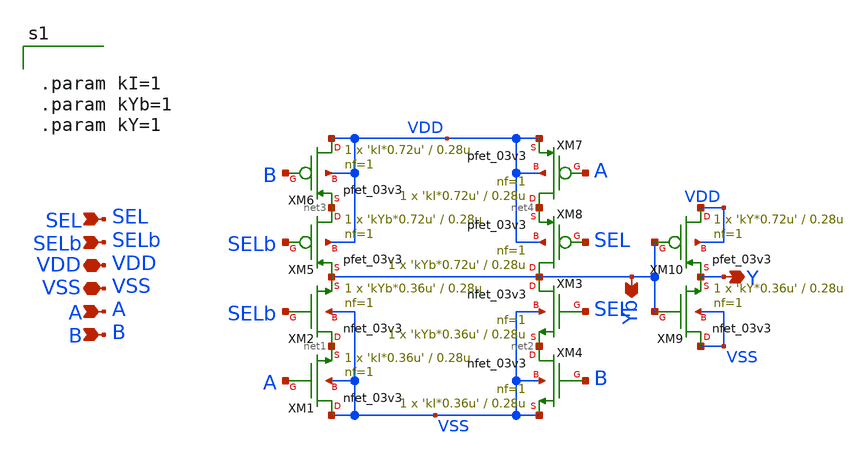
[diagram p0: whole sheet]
** sch_path: CAD4/2x1_mux_cmos.sch
**.subckt 2x1_mux_cmos A B SEL Y VDD VSS SELb Yb
*.ipin A
*.ipin B
*.ipin SEL
*.opin Y
*.iopin VDD
*.iopin VSS
*.ipin SELb
*.opin Yb
XM1 VSS A net1 VSS nfet_03v3 L=0.28u W='kI*0.36u' nf=1 ad='int((nf+1)/2) * W/nf * 0.18u' as='int((nf+2)/2) * W/nf * 0.18u'
+ pd='2*int((nf+1)/2) * (W/nf + 0.18u)' ps='2*int((nf+2)/2) * (W/nf + 0.18u)' nrd='0.18u / W' nrs='0.18u / W'
+ sa=0 sb=0 sd=0 m=1
XM2 net1 SELb Yb VSS nfet_03v3 L=0.28u W='kYb*0.36u' nf=1 ad='int((nf+1)/2) * W/nf * 0.18u' as='int((nf+2)/2) * W/nf * 0.18u'
+ pd='2*int((nf+1)/2) * (W/nf + 0.18u)' ps='2*int((nf+2)/2) * (W/nf + 0.18u)' nrd='0.18u / W' nrs='0.18u / W'
+ sa=0 sb=0 sd=0 m=1
XM3 Yb SEL net2 VSS nfet_03v3 L=0.28u W='kYb*0.36u' nf=1 ad='int((nf+1)/2) * W/nf * 0.18u' as='int((nf+2)/2) * W/nf * 0.18u'
+ pd='2*int((nf+1)/2) * (W/nf + 0.18u)' ps='2*int((nf+2)/2) * (W/nf + 0.18u)' nrd='0.18u / W' nrs='0.18u / W'
+ sa=0 sb=0 sd=0 m=1
XM4 net2 B VSS VSS nfet_03v3 L=0.28u W='kI*0.36u' nf=1 ad='int((nf+1)/2) * W/nf * 0.18u' as='int((nf+2)/2) * W/nf * 0.18u'
+ pd='2*int((nf+1)/2) * (W/nf + 0.18u)' ps='2*int((nf+2)/2) * (W/nf + 0.18u)' nrd='0.18u / W' nrs='0.18u / W'
+ sa=0 sb=0 sd=0 m=1
XM5 net3 SELb Yb VDD pfet_03v3 L=0.28u W='kYb*0.72u' nf=1 ad='int((nf+1)/2) * W/nf * 0.18u' as='int((nf+2)/2) * W/nf * 0.18u'
+ pd='2*int((nf+1)/2) * (W/nf + 0.18u)' ps='2*int((nf+2)/2) * (W/nf + 0.18u)' nrd='0.18u / W' nrs='0.18u / W'
+ sa=0 sb=0 sd=0 m=1
XM6 VDD B net3 VDD pfet_03v3 L=0.28u W='kI*0.72u' nf=1 ad='int((nf+1)/2) * W/nf * 0.18u' as='int((nf+2)/2) * W/nf * 0.18u'
+ pd='2*int((nf+1)/2) * (W/nf + 0.18u)' ps='2*int((nf+2)/2) * (W/nf + 0.18u)' nrd='0.18u / W' nrs='0.18u / W'
+ sa=0 sb=0 sd=0 m=1
XM7 net4 A VDD VDD pfet_03v3 L=0.28u W='kI*0.72u' nf=1 ad='int((nf+1)/2) * W/nf * 0.18u' as='int((nf+2)/2) * W/nf * 0.18u'
+ pd='2*int((nf+1)/2) * (W/nf + 0.18u)' ps='2*int((nf+2)/2) * (W/nf + 0.18u)' nrd='0.18u / W' nrs='0.18u / W'
+ sa=0 sb=0 sd=0 m=1
XM8 Yb SEL net4 VDD pfet_03v3 L=0.28u W='kYb*0.72u' nf=1 ad='int((nf+1)/2) * W/nf * 0.18u' as='int((nf+2)/2) * W/nf * 0.18u'
+ pd='2*int((nf+1)/2) * (W/nf + 0.18u)' ps='2*int((nf+2)/2) * (W/nf + 0.18u)' nrd='0.18u / W' nrs='0.18u / W'
+ sa=0 sb=0 sd=0 m=1
XM9 VSS Yb Y VSS nfet_03v3 L=0.28u W='kY*0.36u' nf=1 ad='int((nf+1)/2) * W/nf * 0.18u' as='int((nf+2)/2) * W/nf * 0.18u'
+ pd='2*int((nf+1)/2) * (W/nf + 0.18u)' ps='2*int((nf+2)/2) * (W/nf + 0.18u)' nrd='0.18u / W' nrs='0.18u / W'
+ sa=0 sb=0 sd=0 m=1
XM10 VDD Yb Y VDD pfet_03v3 L=0.28u W='kY*0.72u' nf=1 ad='int((nf+1)/2) * W/nf * 0.18u' as='int((nf+2)/2) * W/nf * 0.18u'
+ pd='2*int((nf+1)/2) * (W/nf + 0.18u)' ps='2*int((nf+2)/2) * (W/nf + 0.18u)' nrd='0.18u / W' nrs='0.18u / W'
+ sa=0 sb=0 sd=0 m=1
**** begin user architecture code


.param kI=1
.param kYb=1
.param kY=1


**** end user architecture code
**.ends
.end
